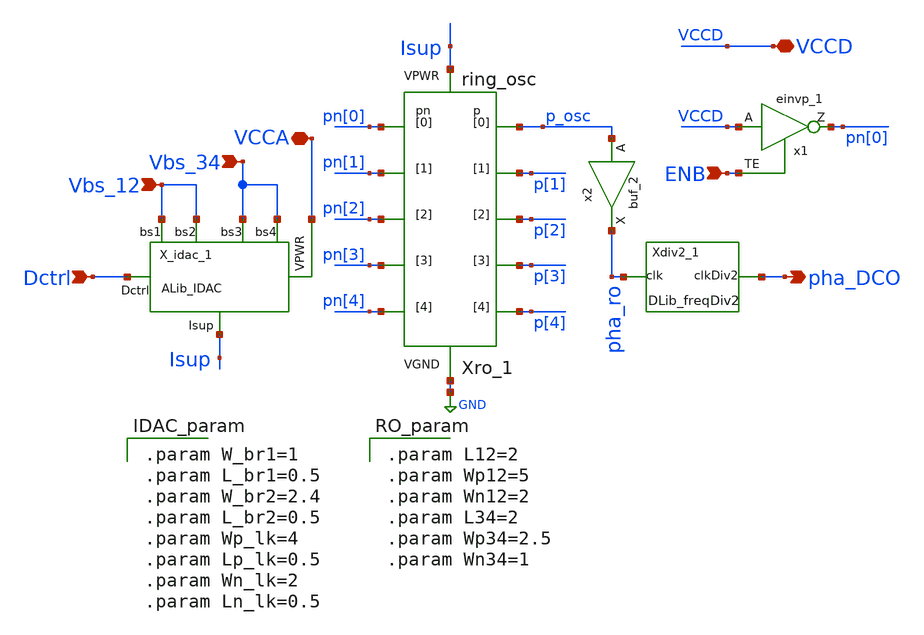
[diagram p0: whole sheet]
** sch_path: xschem/lib/ALib_DCO.sch
**.subckt ALib_DCO Dctrl Vbs_12 Vbs_34 VCCA pha_DCO VCCD ENB
*.ipin Dctrl
*.ipin Vbs_12
*.ipin Vbs_34
*.iopin VCCA
*.opin pha_DCO
*.iopin VCCD
*.ipin ENB
x1 VCCD ENB VGND VNB VPB VPWR pn[0] sky130_fd_sc_hd__einvp_1
Xro_1 GND Isup p_osc p[1] p[2] p[3] p[4] pn[0] pn[1] pn[2] pn[3] pn[4] ring_osc L12="L12"
+ Wp12="Wp12" Wn12="Wn12" L34="L34" Wp34="Wp34" Wn34="Wn34"
X_idac_1 Dctrl Vbs_12 Vbs_12 Vbs_34 Vbs_34 VCCA Isup ALib_IDAC W_br1="W_br1" L_br1="L_br1"
+ W_br2="W_br2" L_br2="L_br2" Wp_lk="Wp_lk" Lp_lk="Lp_lk" Wn_lk="Wn_lk" Ln_lk="Wn_lk"
x2 p_osc GND GND VCCD VCCD pha_ro sky130_fd_sc_hd__buf_2
Xdiv2_1 pha_ro GND GND VCCD VCCD pha_DCO DLib_freqDiv2
**** begin user architecture code

.param W_br1=1
.param L_br1=0.5
.param W_br2=2.4
.param L_br2=0.5
.param Wp_lk=4
.param Lp_lk=0.5
.param Wn_lk=2
.param Ln_lk=0.5


.param L12=2
.param Wp12=5
.param Wn12=2
.param L34=2
.param Wp34=2.5
.param Wn34=1

**** end user architecture code
**.ends
.GLOBAL GND
.end
